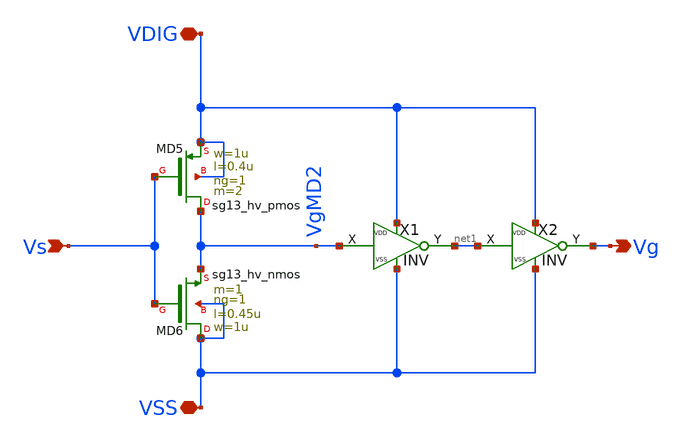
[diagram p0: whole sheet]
** sch_path: xschem/LSHL/LSHL_vto1p1.sch
**.subckt LSHL_vto1p1 VDIG Vs Vg VSS
*.iopin VDIG
*.ipin Vs
*.opin Vg
*.iopin VSS
XMD5 VgMD2 Vs VDIG VDIG sg13_hv_pmos w=1u l=0.4u ng=1 m=2 mm_ok=1
XMD6 VSS Vs VgMD2 VSS sg13_hv_nmos w=1u l=0.45u ng=1 m=1 mm_ok=1
X1 VgMD2 net1 VDIG VSS INV
X2 net1 Vg VDIG VSS INV
**.ends

* expanding   symbol:  ../DigitalGates/INV.sym # of pins=4
** sym_path: xschem/DigitalGates/INV.sym
** sch_path: xschem/DigitalGates/INV.sch
.subckt INV X Y VDD VSS
*.iopin VDD
*.ipin X
*.opin Y
*.iopin VSS
XM3 Y X VSS VSS sg13_lv_nmos w={w_inv} l={l_inv} ng=1 m={mult} mm_ok=1
XM4 Y X VDD VDD sg13_lv_pmos w={w_inv} l={l_inv} ng=1 m={mult*3} mm_ok=1
**** begin user architecture code



**** end user architecture code
.ends

.end
